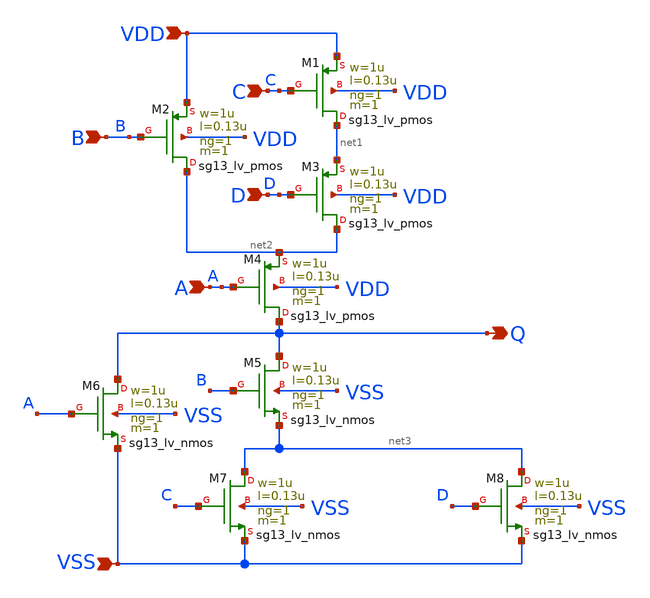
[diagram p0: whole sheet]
** sch_path: Modulo_Digital/Lab1/cmos_funct3.sch
**.subckt cmos_funct3 Q B C D A VDD VSS
*.opin Q
*.ipin B
*.ipin C
*.ipin D
*.ipin A
*.ipin VDD
*.ipin VSS
XM1 net1 C VDD VDD sg13_lv_pmos w=1u l=0.13u ng=1 m=1 mm_ok=1
XM2 net2 B VDD VDD sg13_lv_pmos w=1u l=0.13u ng=1 m=1 mm_ok=1
XM3 net2 D net1 VDD sg13_lv_pmos w=1u l=0.13u ng=1 m=1 mm_ok=1
XM4 Q A net2 VDD sg13_lv_pmos w=1u l=0.13u ng=1 m=1 mm_ok=1
XM5 Q B net3 VSS sg13_lv_nmos w=1u l=0.13u ng=1 m=1 mm_ok=1
XM6 Q A VSS VSS sg13_lv_nmos w=1u l=0.13u ng=1 m=1 mm_ok=1
XM7 net3 C VSS VSS sg13_lv_nmos w=1u l=0.13u ng=1 m=1 mm_ok=1
XM8 net3 D VSS VSS sg13_lv_nmos w=1u l=0.13u ng=1 m=1 mm_ok=1
**.ends
.end
